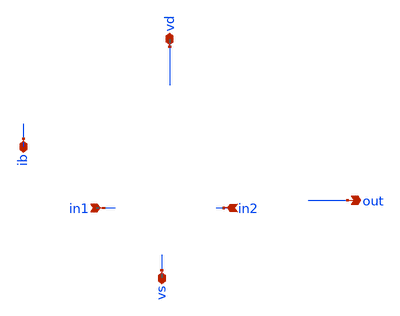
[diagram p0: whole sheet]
** sch_path: xschem/ota-pex.sch
* Copyright 2020 Stefan Frederik Schippers
* Licensed under the Apache License, Version 2.0 (the "License");
* you may not use this file except in compliance with the License.
* You may obtain a copy of the License at
* https://www.apache.org/licenses/LICENSE-2.0
* Unless required by applicable law or agreed to in writing, software
* distributed under the License is distributed on an "AS IS" BASIS,
* WITHOUT WARRANTIES OR CONDITIONS OF ANY KIND, either express or implied.
* See the License for the specific language governing permissions and
* limitations under the License.
**.subckt ota-pex vd vs ib in1 in2 out
*.iopin vd
*.iopin vs
*.iopin ib
*.ipin in1
*.ipin in2
*.opin out
**** begin user architecture code


** NGSPICE file created from ota.ext - technology: sky130A

*.subckt ota ib inn inp out vs vd
X0 out.t12 ib.t4 vd.t39 vd.t38 sky130_fd_pr__pfet_01v8 ad=0p pd=0u as=0p ps=0u w=3e+06u l=1e+06u
X1 vd.t37 ib.t0 ib.t1 vd.t36 sky130_fd_pr__pfet_01v8 ad=0p pd=0u as=0p ps=0u w=3e+06u l=1e+06u
X2 b.t14 inn.t0 c vd.t40 sky130_fd_pr__pfet_01v8 ad=0p pd=0u as=1.92e+12p ps=1.328e+07u w=3e+06u
+ l=150000u
X3 b.t9 ib.t5 vd.t25 vd.t24 sky130_fd_pr__pfet_01v8 ad=0p pd=0u as=0p ps=0u w=3e+06u l=1e+06u
X4 d.t2 c vs.t9 vs.t8 sky130_fd_pr__nfet_01v8 ad=0p pd=0u as=0p ps=0u w=1e+06u l=1e+06u
X5 c inn.t1 b.t13 vd.t43 sky130_fd_pr__pfet_01v8 ad=0p pd=0u as=0p ps=0u w=3e+06u l=150000u
X6 vd.t35 ib.t6 out.t11 vd.t34 sky130_fd_pr__pfet_01v8 ad=0p pd=0u as=0p ps=0u w=3e+06u l=1e+06u
X7 b.t11 inp.t0 d.t4 vd.t44 sky130_fd_pr__pfet_01v8 ad=0p pd=0u as=0p ps=0u w=3e+06u l=150000u
X8 out.t1 d.t5 vs.t3 vs.t2 sky130_fd_pr__nfet_01v8 ad=0p pd=0u as=0p ps=0u w=1e+06u l=1e+06u
X9 out.t10 ib.t7 vd.t29 vd.t28 sky130_fd_pr__pfet_01v8 ad=0p pd=0u as=0p ps=0u w=3e+06u l=1e+06u
X10 out.t9 ib.t8 vd.t33 vd.t32 sky130_fd_pr__pfet_01v8 ad=0p pd=0u as=0p ps=0u w=3e+06u l=1e+06u
X11 vs.t27 d.t6 out.t17 vs.t26 sky130_fd_pr__nfet_01v8 ad=0p pd=0u as=0p ps=0u w=1e+06u l=1e+06u
X12 b.t8 ib.t9 vd.t31 vd.t30 sky130_fd_pr__pfet_01v8 ad=0p pd=0u as=0p ps=0u w=3e+06u l=1e+06u
X13 vd.t27 ib.t10 out.t8 vd.t26 sky130_fd_pr__pfet_01v8 ad=0p pd=0u as=0p ps=0u w=3e+06u l=1e+06u
X14 c inn.t2 b.t12 vd.t9 sky130_fd_pr__pfet_01v8 ad=0p pd=0u as=0p ps=0u w=3e+06u l=150000u
X15 vs.t23 d.t7 out.t15 vs.t22 sky130_fd_pr__nfet_01v8 ad=0p pd=0u as=0p ps=0u w=1e+06u l=1e+06u
X16 out.t16 d.t8 vs.t25 vs.t24 sky130_fd_pr__nfet_01v8 ad=0p pd=0u as=0p ps=0u w=1e+06u l=1e+06u
X17 vd.t23 ib.t11 b.t7 vd.t22 sky130_fd_pr__pfet_01v8 ad=0p pd=0u as=0p ps=0u w=3e+06u l=1e+06u
X18 b.t6 b.t4 b.t5 vd.t45 sky130_fd_pr__pfet_01v8 ad=0p pd=0u as=0p ps=0u w=3e+06u l=150000u
X19 out.t7 ib.t12 vd.t21 vd.t20 sky130_fd_pr__pfet_01v8 ad=0p pd=0u as=0p ps=0u w=3e+06u l=1e+06u
X20 d.t0 inp.t1 b.t0 vd.t0 sky130_fd_pr__pfet_01v8 ad=0p pd=0u as=0p ps=0u w=3e+06u l=150000u
X21 vd.t19 ib.t13 out.t6 vd.t18 sky130_fd_pr__pfet_01v8 ad=0p pd=0u as=0p ps=0u w=3e+06u l=1e+06u
X22 vs.t19 vs.t16 vs.t18 vs.t17 sky130_fd_pr__nfet_01v8 ad=0p pd=0u as=0p ps=0u w=1e+06u l=1e+06u
X23 vd.t17 ib.t14 out.t5 vd.t16 sky130_fd_pr__pfet_01v8 ad=0p pd=0u as=0p ps=0u w=3e+06u l=1e+06u
X24 vd.t8 vd.t5 vd.t7 vd.t6 sky130_fd_pr__pfet_01v8 ad=0p pd=0u as=0p ps=0u w=3e+06u l=1e+06u
X25 vs.t1 d.t9 out.t0 vs.t0 sky130_fd_pr__nfet_01v8 ad=0p pd=0u as=0p ps=0u w=1e+06u l=1e+06u
X26 out.t19 d.t1 sky130_fd_pr__cap_mim_m3_1 l=1.4e+07u w=2.4e+07u
X27 ib.t3 ib.t2 vd.t13 vd.t12 sky130_fd_pr__pfet_01v8 ad=0p pd=0u as=0p ps=0u w=3e+06u l=1e+06u
X28 b.t10 inp.t2 d.t3 vd.t41 sky130_fd_pr__pfet_01v8 ad=0p pd=0u as=0p ps=0u w=3e+06u l=150000u
X29 b.t3 b.t1 b.t2 vd.t42 sky130_fd_pr__pfet_01v8 ad=0p pd=0u as=0p ps=0u w=3e+06u l=150000u
X30 vd.t15 ib.t15 out.t4 vd.t14 sky130_fd_pr__pfet_01v8 ad=0p pd=0u as=0p ps=0u w=3e+06u l=1e+06u
X31 out.t13 d.t10 vs.t11 vs.t10 sky130_fd_pr__nfet_01v8 ad=0p pd=0u as=0p ps=0u w=1e+06u l=1e+06u
X32 out.t3 ib.t16 vd.t11 vd.t10 sky130_fd_pr__pfet_01v8 ad=0p pd=0u as=0p ps=0u w=3e+06u l=1e+06u
X33 vs.t7 c c vs.t6 sky130_fd_pr__nfet_01v8 ad=0p pd=0u as=2.9e+11p ps=2.58e+06u w=1e+06u l=1e+06u
X34 vs.t21 d.t11 out.t14 vs.t20 sky130_fd_pr__nfet_01v8 ad=0p pd=0u as=0p ps=0u w=1e+06u l=1e+06u
X35 vs.t29 d.t12 out.t18 vs.t28 sky130_fd_pr__nfet_01v8 ad=0p pd=0u as=0p ps=0u w=1e+06u l=1e+06u
X36 vd.t4 vd.t1 vd.t3 vd.t2 sky130_fd_pr__pfet_01v8 ad=0p pd=0u as=0p ps=0u w=3e+06u l=1e+06u
X37 out.t2 d.t13 vs.t5 vs.t4 sky130_fd_pr__nfet_01v8 ad=0p pd=0u as=0p ps=0u w=1e+06u l=1e+06u
X38 vs.t15 vs.t12 vs.t14 vs.t13 sky130_fd_pr__nfet_01v8 ad=0p pd=0u as=0p ps=0u w=1e+06u l=1e+06u
R0 ib.n1 ib.t6 88.265
R1 ib.n15 ib.t2 87.728
R2 ib.n13 ib.t0 87.728
R3 ib.n12 ib.t5 87.728
R4 ib.n11 ib.t11 87.728
R5 ib.n10 ib.t9 87.728
R6 ib.n9 ib.t7 87.728
R7 ib.n8 ib.t13 87.728
R8 ib.n7 ib.t12 87.728
R9 ib.n6 ib.t14 87.728
R10 ib.n5 ib.t16 87.728
R11 ib.n4 ib.t15 87.728
R12 ib.n3 ib.t4 87.728
R13 ib.n2 ib.t10 87.728
R14 ib.n1 ib.t8 87.728
R15 ib.n0 ib.t1 9.521
R16 ib.n0 ib.t3 9.521
R17 ib ib.n15 2.069
R18 ib.n10 ib.n9 0.8
R19 ib.n13 ib.n12 0.795
R20 ib.n14 ib.n0 0.604
R21 ib.n2 ib.n1 0.537
R22 ib.n3 ib.n2 0.537
R23 ib.n4 ib.n3 0.537
R24 ib.n5 ib.n4 0.537
R25 ib.n6 ib.n5 0.537
R26 ib.n7 ib.n6 0.537
R27 ib.n8 ib.n7 0.537
R28 ib.n9 ib.n8 0.537
R29 ib.n11 ib.n10 0.537
R30 ib.n12 ib.n11 0.537
R31 ib.n14 ib.n13 0.275
R32 ib.n15 ib.n14 0.262
R33 vd.n19 vd.n18 465.543
R34 vd.n24 vd.n21 342.4
R35 vd.n18 vd.t6 112.812
R36 vd.t32 vd.t34 109.419
R37 vd.t26 vd.t32 109.419
R38 vd.t38 vd.t26 109.419
R39 vd.t14 vd.t38 109.419
R40 vd.t10 vd.t14 109.419
R41 vd.t16 vd.t10 109.419
R42 vd.t18 vd.t28 109.419
R43 vd.t22 vd.t30 109.419
R44 vd.n23 vd.t1 87.728
R45 vd.n1 vd.t5 87.728
R46 vd.t45 vd.t12 86.941
R47 vd.t24 vd.t42 74.218
R48 vd.n14 vd.t2 70.401
R49 vd.t36 vd.t41 68.281
R50 vd.n21 vd.t18 54.285
R51 vd.n20 vd.t20 50.892
R52 vd.n16 vd.n15 50.604
R53 vd.n21 vd.n19 50.603
R54 vd.t0 vd.t44 40.714
R55 vd.t41 vd.t0 40.714
R56 vd.t40 vd.t43 40.714
R57 vd.t9 vd.t40 40.714
R58 vd.t42 vd.t22 35.2
R59 vd.t43 vd.t36 19.933
R60 vd.n17 vd.t16 16.116
R61 vd.t44 vd.t24 12.299
R62 vd.n22 vd.t3 10.333
R63 vd.n22 vd.t4 10.305
R64 vd.n6 vd.t35 10.257
R65 vd.n13 vd.t37 10.06
R66 vd.n0 vd.t7 10.039
R67 vd.n0 vd.t8 10.016
R68 vd.n10 vd.t29 9.612
R69 vd.n12 vd.t25 9.558
R70 vd.n13 vd.t13 9.523
R71 vd.n11 vd.t31 9.521
R72 vd.n11 vd.t23 9.521
R73 vd.n5 vd.t33 9.521
R74 vd.n5 vd.t27 9.521
R75 vd.n4 vd.t39 9.521
R76 vd.n4 vd.t15 9.521
R77 vd.n3 vd.t11 9.521
R78 vd.n3 vd.t17 9.521
R79 vd.n2 vd.t21 9.521
R80 vd.n2 vd.t19 9.521
R81 vd.t12 vd.t9 8.058
R82 vd.n21 vd.n20 4.241
R83 vd.n14 vd.t45 3.816
R84 vd.n28 vd.n1 2.393
R85 vd.n27 vd.n26 0.937
R86 vd.n25 vd.n13 0.768
R87 vd.n27 vd.n10 0.733
R88 vd.n26 vd.n12 0.731
R89 vd.n26 vd.n25 0.666
R90 vd.n7 vd.n6 0.645
R91 vd.n8 vd.n7 0.645
R92 vd.n9 vd.n8 0.645
R93 vd.n10 vd.n9 0.645
R94 vd.n12 vd.n11 0.574
R95 vd.n28 vd.n27 0.5
R96 vd vd.n28 0.172
R97 vd.n6 vd.n5 0.091
R98 vd.n7 vd.n4 0.091
R99 vd.n8 vd.n3 0.091
R100 vd.n9 vd.n2 0.091
R101 vd.n24 vd.n23 0.084
R102 vd.n1 vd.n0 0.071
R103 vd.n25 vd.n24 0.062
R104 vd.n23 vd.n22 0.003
R105 vd.n19 vd.n17 0.001
R106 vd.n16 vd.n14 0.001
R107 vd.n24 vd.n16 0.001
R108 out.n10 out.t14 19.093
R109 out.n9 out.t15 17.4
R110 out.n9 out.t13 17.4
R111 out.n11 out.t17 17.4
R112 out.n11 out.t16 17.4
R113 out.n13 out.t0 17.4
R114 out.n13 out.t1 17.4
R115 out.n15 out.t18 17.4
R116 out.n15 out.t2 17.4
R117 out.n0 out.t8 9.521
R118 out.n0 out.t12 9.521
R119 out.n1 out.t4 9.521
R120 out.n1 out.t3 9.521
R121 out.n2 out.t5 9.521
R122 out.n2 out.t7 9.521
R123 out.n3 out.t6 9.521
R124 out.n3 out.t10 9.521
R125 out.n7 out.t11 9.521
R126 out.n7 out.t9 9.521
R127 out.n17 out.n16 2.528
R128 out.n12 out.n10 1.468
R129 out.n14 out.n12 1.468
R130 out out.n17 1.334
R131 out.n16 out.n14 1.056
R132 out.n4 out.n3 0.651
R133 out.n16 out.t19 0.627
R134 out.n6 out.n5 0.586
R135 out.n5 out.n4 0.586
R136 out.n8 out.n6 0.408
R137 out.n17 out.n8 0.381
R138 out.n16 out.n15 0.372
R139 out.n8 out.n7 0.18
R140 out.n10 out.n9 0.16
R141 out.n12 out.n11 0.16
R142 out.n14 out.n13 0.16
R143 out.n6 out.n0 0.064
R144 out.n5 out.n1 0.064
R145 out.n4 out.n2 0.064
R146 inn.n0 inn.t2 580.203
R147 inn.n0 inn.t1 580.093
R148 inn inn.t0 571.806
R149 inn.t0 inn.n0 514.133
R150 b.n4 b.t1 569.466
R151 b.n7 b.t4 569.42
R152 b.n6 b.t11 10.837
R153 b.n9 b.t12 10.837
R154 b.n0 b.t0 10.835
R155 b.n0 b.t10 10.835
R156 b.n1 b.t13 10.835
R157 b.n1 b.t14 10.835
R158 b.n7 b.t6 10.194
R159 b.n8 b.t5 10.01
R160 b.n4 b.t2 9.828
R161 b.n5 b.t3 9.792
R162 b.n3 b.t8 9.741
R163 b.n2 b.t7 9.521
R164 b.n2 b.t9 9.521
R165 b b.n3 1.28
R166 b b.n10 0.458
R167 b.n8 b.n7 0.23
R168 b.n3 b.n2 0.188
R169 b.n0 b.n6 0.15
R170 b.n1 b.n9 0.15
R171 b.n10 b.n1 0.121
R172 b.n10 b.n0 0.119
R173 b.n9 b.n8 0.106
R174 b.n6 b.n5 0.091
R175 b.n5 b.n4 0.036
R176 vs.t6 vs.t8 1892.47
R177 vs.t17 vs.t28 1778.92
R178 vs.n17 vs.t6 1741.07
R179 vs.t0 vs.t4 1220.65
R180 vs.t2 vs.t0 1220.65
R181 vs.t24 vs.t22 1220.65
R182 vs.t22 vs.t10 1220.65
R183 vs.t10 vs.t20 1220.65
R184 vs.n21 vs.t24 1078.71
R185 vs.n19 vs.t17 784.766
R186 vs.n20 vs.n19 401.137
R187 vs.n23 vs.n22 324.515
R188 vs.n18 vs.t2 132.473
R189 vs.n22 vs.t26 94.623
R190 vs.n16 vs.n15 75.12
R191 vs.n17 vs.t13 56.774
R192 vs.n22 vs.n21 47.311
R193 vs.n26 vs.n16 40.001
R194 vs.n22 vs.n20 37.561
R195 vs.n9 vs.t16 37.359
R196 vs.n25 vs.t12 37.359
R197 vs.n9 vs.t18 17.683
R198 vs.n10 vs.t19 17.672
R199 vs.n8 vs.t29 17.544
R200 vs.n24 vs.t15 17.428
R201 vs.n24 vs.t14 17.426
R202 vs.n0 vs.t7 17.404
R203 vs.n0 vs.t9 17.404
R204 vs.n1 vs.t11 17.4
R205 vs.n1 vs.t21 17.4
R206 vs.n2 vs.t25 17.4
R207 vs.n2 vs.t23 17.4
R208 vs.n4 vs.t3 17.4
R209 vs.n4 vs.t27 17.4
R210 vs.n6 vs.t5 17.4
R211 vs.n6 vs.t1 17.4
R212 vs.n12 vs.n11 2.901
R213 vs.n3 vs.n1 1.618
R214 vs.n5 vs.n3 1.468
R215 vs.n7 vs.n5 1.468
R216 vs.n8 vs.n7 1.468
R217 vs.n11 vs.n8 1.381
R218 vs.n12 vs.n0 1.039
R219 vs vs.n27 0.614
R220 vs.n27 vs.n12 0.447
R221 vs.n11 vs.n10 0.178
R222 vs.n3 vs.n2 0.15
R223 vs.n5 vs.n4 0.15
R224 vs.n7 vs.n6 0.15
R225 vs.n26 vs.n25 0.097
R226 vs.n25 vs.n24 0.061
R227 vs.n27 vs.n26 0.037
R228 vs.n10 vs.n9 0.002
R229 vs.n16 vs.n14 0.001
R230 vs.n14 vs.n13 0.001
R231 vs.n20 vs.n18 0.001
R232 vs.n26 vs.n23 0.001
R233 vs.n23 vs.n17 0.001
R234 d.n3 d.t12 38.045
R235 d.n10 d.t11 37.359
R236 d.n9 d.t10 37.359
R237 d.n8 d.t7 37.359
R238 d.n7 d.t8 37.359
R239 d.n6 d.t6 37.359
R240 d.n5 d.t5 37.359
R241 d.n4 d.t9 37.359
R242 d.n3 d.t13 37.359
R243 d.n2 d.t2 17.404
R244 d.n1 d.t3 10.964
R245 d.n0 d.t4 10.835
R246 d.n0 d.t0 10.835
R247 d d.n1 1.969
R248 d.n2 d.t1 1.881
R249 d.n4 d.n3 0.686
R250 d.n5 d.n4 0.686
R251 d.n6 d.n5 0.686
R252 d.n7 d.n6 0.686
R253 d.n8 d.n7 0.686
R254 d.n9 d.n8 0.686
R255 d.n10 d.n9 0.686
R256 d.n11 d.n10 0.621
R257 d.n11 d.n2 0.274
R258 d d.n11 0.156
R259 d.n1 d.n0 0.113
R260 inp.n0 inp.t0 585.4
R261 inp.n1 inp.t2 536.042
R262 inp.n0 inp.t1 514.133
R263 inp.n1 inp.n0 50.61
R264 inp inp.n1 25.257
C0 out ib 2.11fF
C1 c vd 0.39fF
C2 b vd 2.28fF
C3 out inn 0.00fF
C4 d out 33.38fF
C5 vd ib 11.60fF
C6 out inp 0.01fF
C7 c b 1.12fF
C8 inn vd 0.46fF
C9 d vd 1.54fF
C10 c ib 0.06fF
C11 inp vd 0.56fF
C12 b ib 1.23fF
C13 inn c 0.22fF
C14 d c 0.77fF
C15 inn b 0.43fF
C16 d b 1.10fF
C17 c inp 0.16fF
C18 b inp 0.28fF
C19 inn ib 1.07fF
C20 d ib 0.14fF
C21 inp ib 0.07fF
C22 d inn 0.01fF
C23 out vd 3.08fF
C24 inn inp 0.10fF
C25 d inp 0.39fF
C26 out c 0.03fF
C27 out b 0.08fF
*.ends



**** end user architecture code
**.ends
.end
